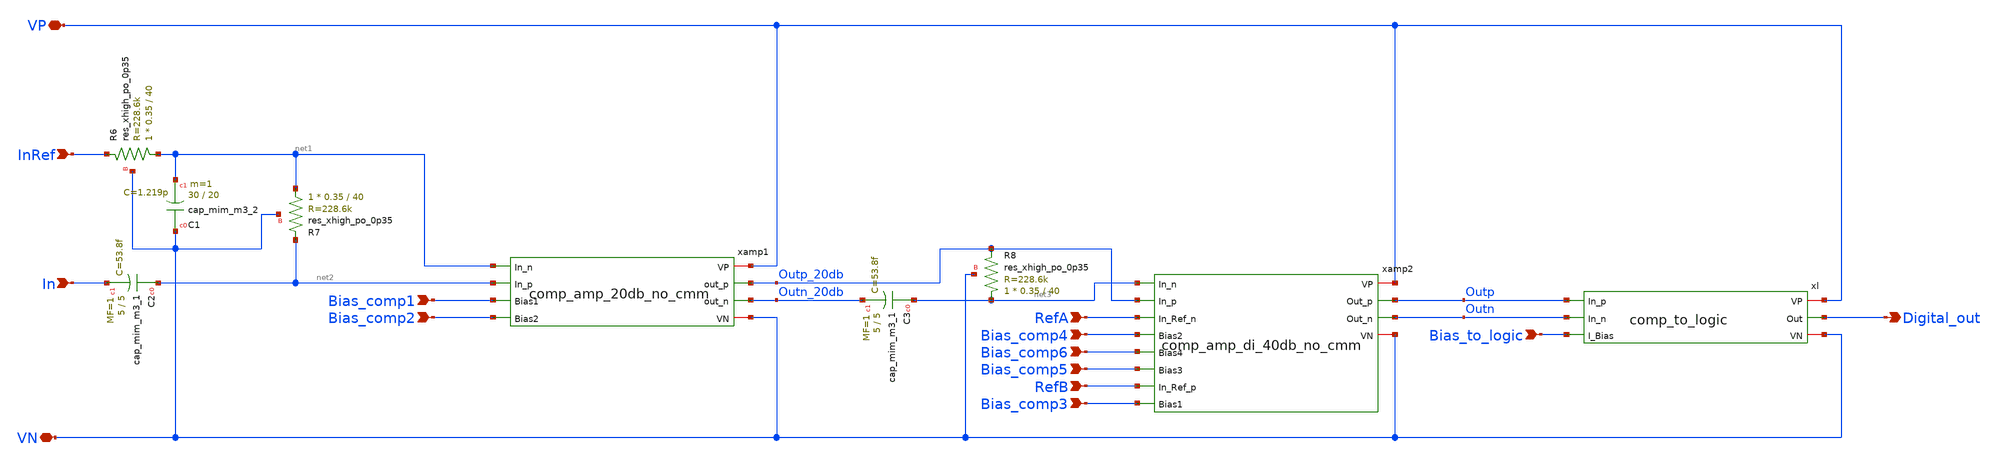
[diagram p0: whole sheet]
** sch_path: xschem/comp/comparator_complete.sch
**.subckt comparator_complete InRef VP Digital_out In Bias_comp1 Bias_comp2 VN Bias_comp4 Bias_comp6
*+ Bias_comp3 Bias_comp5 RefA RefB Bias_to_logic
*.ipin InRef
*.iopin VP
*.opin Digital_out
*.ipin In
*.ipin Bias_comp1
*.ipin Bias_comp2
*.iopin VN
*.ipin Bias_comp4
*.ipin Bias_comp6
*.ipin Bias_comp3
*.ipin Bias_comp5
*.ipin RefA
*.ipin RefB
*.ipin Bias_to_logic
xamp1 VP net1 net2 Outp_20db Bias_comp1 Bias_comp2 Outn_20db VN comp_amp_20db_no_cmm
xl VP Digital_out Outp Outn Bias_to_logic VN comp_to_logic
xamp2 VP net3 Outp_20db Outp RefA Bias_comp4 Bias_comp6 Bias_comp5 Outn RefB Bias_comp3 VN
+ comp_amp_di_40db_no_cmm
XR6 net1 InRef VN sky130_fd_pr__res_xhigh_po_0p35 L=40 mult=1 m=1
XR7 net1 net2 VN sky130_fd_pr__res_xhigh_po_0p35 L=40 mult=1 m=1
XR8 net3 Outp_20db VN sky130_fd_pr__res_xhigh_po_0p35 L=40 mult=1 m=1
XC1 VN net1 sky130_fd_pr__cap_mim_m3_2 W=30 L=20 MF=1 m=1
XC2 net2 In sky130_fd_pr__cap_mim_m3_1 W=5 L=5 MF=1 m=1
XC3 net3 Outn_20db sky130_fd_pr__cap_mim_m3_1 W=5 L=5 MF=1 m=1
**.ends

* expanding   symbol:  comp/comp_amp_20db_no_cmm.sym # of pins=8
** sym_path: xschem/comp/comp_amp_20db_no_cmm.sym
** sch_path: xschem/comp/comp_amp_20db_no_cmm.sch
.subckt comp_amp_20db_no_cmm VP In_n In_p out_p Bias1 Bias2 out_n VN
*.ipin In_n
*.ipin In_p
*.iopin VP
*.opin out_p
*.opin out_n
*.ipin Bias1
*.ipin Bias2
*.iopin VN
xcmp2 VP out_p out_n OutP1 OutN1 Bias2 VN comp_adv3
xcmp1 VP OutP1 OutN1 In_n In_p Bias1 VN comp_adv3
.ends


* expanding   symbol:  comp/comp_to_logic.sym # of pins=6
** sym_path: xschem/comp/comp_to_logic.sym
** sch_path: xschem/comp/comp_to_logic.sch
.subckt comp_to_logic VP Out In_p In_n I_Bias VN
*.iopin VP
*.iopin VN
*.ipin In_p
*.ipin In_n
*.ipin I_Bias
*.opin Out
XM1 VM1D In_n VM4D VN sky130_fd_pr__nfet_01v8_lvt L=0.15 W=2 nf=1 ad='int((nf+1)/2) * W/nf * 0.29' as='int((nf+2)/2) * W/nf * 0.29'
+ pd='2*int((nf+1)/2) * (W/nf + 0.29)' ps='2*int((nf+2)/2) * (W/nf + 0.29)' nrd='0.29 / W' nrs='0.29 / W'
+ sa=0 sb=0 sd=0 mult=2 m=2
XM2 VM1D VM1D VP VP sky130_fd_pr__pfet_01v8 L=0.15 W=2 nf=1 ad='int((nf+1)/2) * W/nf * 0.29' as='int((nf+2)/2) * W/nf * 0.29'
+ pd='2*int((nf+1)/2) * (W/nf + 0.29)' ps='2*int((nf+2)/2) * (W/nf + 0.29)' nrd='0.29 / W' nrs='0.29 / W'
+ sa=0 sb=0 sd=0 mult=2 m=2
XM4 VM4D I_Bias VN VN sky130_fd_pr__nfet_01v8 L=0.3 W=2 nf=1 ad='int((nf+1)/2) * W/nf * 0.29' as='int((nf+2)/2) * W/nf * 0.29'
+ pd='2*int((nf+1)/2) * (W/nf + 0.29)' ps='2*int((nf+2)/2) * (W/nf + 0.29)' nrd='0.29 / W' nrs='0.29 / W'
+ sa=0 sb=0 sd=0 mult=2*8 m=2*8
XM6 VM6D In_p VM4D VN sky130_fd_pr__nfet_01v8_lvt L=0.15 W=2 nf=1 ad='int((nf+1)/2) * W/nf * 0.29' as='int((nf+2)/2) * W/nf * 0.29'
+ pd='2*int((nf+1)/2) * (W/nf + 0.29)' ps='2*int((nf+2)/2) * (W/nf + 0.29)' nrd='0.29 / W' nrs='0.29 / W'
+ sa=0 sb=0 sd=0 mult=2 m=2
XM7 I_Bias I_Bias VN VN sky130_fd_pr__nfet_01v8 L=0.3 W=2 nf=1 ad='int((nf+1)/2) * W/nf * 0.29' as='int((nf+2)/2) * W/nf * 0.29'
+ pd='2*int((nf+1)/2) * (W/nf + 0.29)' ps='2*int((nf+2)/2) * (W/nf + 0.29)' nrd='0.29 / W' nrs='0.29 / W'
+ sa=0 sb=0 sd=0 mult=2 m=2
XM3 VM6D VM6D VP VP sky130_fd_pr__pfet_01v8 L=0.15 W=2 nf=1 ad='int((nf+1)/2) * W/nf * 0.29' as='int((nf+2)/2) * W/nf * 0.29'
+ pd='2*int((nf+1)/2) * (W/nf + 0.29)' ps='2*int((nf+2)/2) * (W/nf + 0.29)' nrd='0.29 / W' nrs='0.29 / W'
+ sa=0 sb=0 sd=0 mult=2 m=2
XM8 VM11D VM1D VP VP sky130_fd_pr__pfet_01v8 L=0.15 W=2 nf=1 ad='int((nf+1)/2) * W/nf * 0.29' as='int((nf+2)/2) * W/nf * 0.29'
+ pd='2*int((nf+1)/2) * (W/nf + 0.29)' ps='2*int((nf+2)/2) * (W/nf + 0.29)' nrd='0.29 / W' nrs='0.29 / W'
+ sa=0 sb=0 sd=0 mult=4 m=4
XM9 VM12D VM6D VP VP sky130_fd_pr__pfet_01v8 L=0.15 W=2 nf=1 ad='int((nf+1)/2) * W/nf * 0.29' as='int((nf+2)/2) * W/nf * 0.29'
+ pd='2*int((nf+1)/2) * (W/nf + 0.29)' ps='2*int((nf+2)/2) * (W/nf + 0.29)' nrd='0.29 / W' nrs='0.29 / W'
+ sa=0 sb=0 sd=0 mult=4 m=4
XM11 VM11D VM11D VN VN sky130_fd_pr__nfet_01v8 L=0.15 W=2 nf=1 ad='int((nf+1)/2) * W/nf * 0.29' as='int((nf+2)/2) * W/nf * 0.29'
+ pd='2*int((nf+1)/2) * (W/nf + 0.29)' ps='2*int((nf+2)/2) * (W/nf + 0.29)' nrd='0.29 / W' nrs='0.29 / W'
+ sa=0 sb=0 sd=0 mult=3 m=3
XM12 VM12D VM11D VN VN sky130_fd_pr__nfet_01v8 L=0.15 W=2 nf=1 ad='int((nf+1)/2) * W/nf * 0.29' as='int((nf+2)/2) * W/nf * 0.29'
+ pd='2*int((nf+1)/2) * (W/nf + 0.29)' ps='2*int((nf+2)/2) * (W/nf + 0.29)' nrd='0.29 / W' nrs='0.29 / W'
+ sa=0 sb=0 sd=0 mult=3 m=3
XM14 VM17D VM12D VP VP sky130_fd_pr__pfet_01v8 L=0.15 W=2 nf=1 ad='int((nf+1)/2) * W/nf * 0.29' as='int((nf+2)/2) * W/nf * 0.29'
+ pd='2*int((nf+1)/2) * (W/nf + 0.29)' ps='2*int((nf+2)/2) * (W/nf + 0.29)' nrd='0.29 / W' nrs='0.29 / W'
+ sa=0 sb=0 sd=0 mult=2 m=2
XM16 VM13D VM17D VP VP sky130_fd_pr__pfet_01v8 L=0.15 W=2 nf=1 ad='int((nf+1)/2) * W/nf * 0.29' as='int((nf+2)/2) * W/nf * 0.29'
+ pd='2*int((nf+1)/2) * (W/nf + 0.29)' ps='2*int((nf+2)/2) * (W/nf + 0.29)' nrd='0.29 / W' nrs='0.29 / W'
+ sa=0 sb=0 sd=0 mult=4 m=4
XM13 VM13D VM17D VN VN sky130_fd_pr__nfet_01v8_lvt L=0.15 W=2 nf=1 ad='int((nf+1)/2) * W/nf * 0.29' as='int((nf+2)/2) * W/nf * 0.29'
+ pd='2*int((nf+1)/2) * (W/nf + 0.29)' ps='2*int((nf+2)/2) * (W/nf + 0.29)' nrd='0.29 / W' nrs='0.29 / W'
+ sa=0 sb=0 sd=0 mult=2 m=2
XM17 VM17D VM12D VN VN sky130_fd_pr__nfet_01v8 L=0.15 W=2 nf=1 ad='int((nf+1)/2) * W/nf * 0.29' as='int((nf+2)/2) * W/nf * 0.29'
+ pd='2*int((nf+1)/2) * (W/nf + 0.29)' ps='2*int((nf+2)/2) * (W/nf + 0.29)' nrd='0.29 / W' nrs='0.29 / W'
+ sa=0 sb=0 sd=0 mult=1 m=1
XM15 VM6D VM1D VP VP sky130_fd_pr__pfet_01v8 L=0.15 W=0.5 nf=1 ad='int((nf+1)/2) * W/nf * 0.29' as='int((nf+2)/2) * W/nf * 0.29'
+ pd='2*int((nf+1)/2) * (W/nf + 0.29)' ps='2*int((nf+2)/2) * (W/nf + 0.29)' nrd='0.29 / W' nrs='0.29 / W'
+ sa=0 sb=0 sd=0 mult=1 m=1
XM19 Out VM13D VP VP sky130_fd_pr__pfet_01v8 L=0.15 W=2 nf=1 ad='int((nf+1)/2) * W/nf * 0.29' as='int((nf+2)/2) * W/nf * 0.29'
+ pd='2*int((nf+1)/2) * (W/nf + 0.29)' ps='2*int((nf+2)/2) * (W/nf + 0.29)' nrd='0.29 / W' nrs='0.29 / W'
+ sa=0 sb=0 sd=0 mult=4 m=4
XM20 Out VM13D VN VN sky130_fd_pr__nfet_01v8_lvt L=0.15 W=2 nf=1 ad='int((nf+1)/2) * W/nf * 0.29' as='int((nf+2)/2) * W/nf * 0.29'
+ pd='2*int((nf+1)/2) * (W/nf + 0.29)' ps='2*int((nf+2)/2) * (W/nf + 0.29)' nrd='0.29 / W' nrs='0.29 / W'
+ sa=0 sb=0 sd=0 mult=2 m=2
XM5 VM1D VM6D VP VP sky130_fd_pr__pfet_01v8 L=0.15 W=0.5 nf=1 ad='int((nf+1)/2) * W/nf * 0.29' as='int((nf+2)/2) * W/nf * 0.29'
+ pd='2*int((nf+1)/2) * (W/nf + 0.29)' ps='2*int((nf+2)/2) * (W/nf + 0.29)' nrd='0.29 / W' nrs='0.29 / W'
+ sa=0 sb=0 sd=0 mult=1 m=1
XM10 VN VN VN VN sky130_fd_pr__nfet_01v8 L=0.3 W=2 nf=1 ad='int((nf+1)/2) * W/nf * 0.29' as='int((nf+2)/2) * W/nf * 0.29'
+ pd='2*int((nf+1)/2) * (W/nf + 0.29)' ps='2*int((nf+2)/2) * (W/nf + 0.29)' nrd='0.29 / W' nrs='0.29 / W'
+ sa=0 sb=0 sd=0 mult=2 m=2
.ends


* expanding   symbol:  comp/comp_amp_di_40db_no_cmm.sym # of pins=12
** sym_path: xschem/comp/comp_amp_di_40db_no_cmm.sym
** sch_path: xschem/comp/comp_amp_di_40db_no_cmm.sch
.subckt comp_amp_di_40db_no_cmm VP In_n In_p Out_p In_Ref_n Bias2 Bias4 Bias3 Out_n In_Ref_p Bias1
+ VN
*.ipin In_n
*.iopin VP
*.opin Out_p
*.ipin In_p
*.ipin Bias1
*.ipin Bias2
*.iopin VN
*.opin Out_n
*.ipin Bias3
*.ipin Bias4
*.ipin In_Ref_n
*.ipin In_Ref_p
xcmp6 VP OutP2_di OutN2_di OutP1_di OutN1_di Bias2 VN comp_adv3
xcmp1 VP OutP3_di OutN3_di OutP2_di OutN2_di Bias3 VN comp_adv3
xcmp2 VP Out_p Out_n OutP3_di OutN3_di Bias4 VN comp_adv3
x1 VP OutP1_di OutN1_di In_n In_p In_Ref_n In_Ref_p Bias1 VN comp_adv3_di
.ends


* expanding   symbol:  comp/comp_adv3.sym # of pins=7
** sym_path: xschem/comp/comp_adv3.sym
** sch_path: xschem/comp/comp_adv3.sch
.subckt comp_adv3 VP OutP OutN Inn Inp bias VN
*.ipin Inp
*.ipin bias
*.ipin Inn
*.iopin VP
*.iopin VN
*.opin OutN
*.opin OutP
XM1 OutN Inp VIq VN sky130_fd_pr__nfet_01v8_lvt L=0.15 W=2 nf=1 ad='int((nf+1)/2) * W/nf * 0.29' as='int((nf+2)/2) * W/nf * 0.29'
+ pd='2*int((nf+1)/2) * (W/nf + 0.29)' ps='2*int((nf+2)/2) * (W/nf + 0.29)' nrd='0.29 / W' nrs='0.29 / W'
+ sa=0 sb=0 sd=0 mult=6 m=6
XM2 OutP Inn VIq VN sky130_fd_pr__nfet_01v8_lvt L=0.15 W=2 nf=1 ad='int((nf+1)/2) * W/nf * 0.29' as='int((nf+2)/2) * W/nf * 0.29'
+ pd='2*int((nf+1)/2) * (W/nf + 0.29)' ps='2*int((nf+2)/2) * (W/nf + 0.29)' nrd='0.29 / W' nrs='0.29 / W'
+ sa=0 sb=0 sd=0 mult=6 m=6
XM7 bias bias VN VN sky130_fd_pr__nfet_01v8_lvt L=0.3 W=2 nf=1 ad='int((nf+1)/2) * W/nf * 0.29' as='int((nf+2)/2) * W/nf * 0.29'
+ pd='2*int((nf+1)/2) * (W/nf + 0.29)' ps='2*int((nf+2)/2) * (W/nf + 0.29)' nrd='0.29 / W' nrs='0.29 / W'
+ sa=0 sb=0 sd=0 mult=1 m=1
XM9 VIq bias VN VN sky130_fd_pr__nfet_01v8_lvt L=0.3 W=2 nf=1 ad='int((nf+1)/2) * W/nf * 0.29' as='int((nf+2)/2) * W/nf * 0.29'
+ pd='2*int((nf+1)/2) * (W/nf + 0.29)' ps='2*int((nf+2)/2) * (W/nf + 0.29)' nrd='0.29 / W' nrs='0.29 / W'
+ sa=0 sb=0 sd=0 mult=10 m=10
XR1 OutN VP VN sky130_fd_pr__res_xhigh_po_2p85 L=1.5 mult=1 m=1
XR2 OutP VP VN sky130_fd_pr__res_xhigh_po_2p85 L=1.5 mult=1 m=1
XM3 bias VN VN VN sky130_fd_pr__nfet_01v8_lvt L=0.3 W=2 nf=1 ad='int((nf+1)/2) * W/nf * 0.29' as='int((nf+2)/2) * W/nf * 0.29'
+ pd='2*int((nf+1)/2) * (W/nf + 0.29)' ps='2*int((nf+2)/2) * (W/nf + 0.29)' nrd='0.29 / W' nrs='0.29 / W'
+ sa=0 sb=0 sd=0 mult=1 m=1
.ends


* expanding   symbol:  comp/comp_adv3_di.sym # of pins=9
** sym_path: xschem/comp/comp_adv3_di.sym
** sch_path: xschem/comp/comp_adv3_di.sch
.subckt comp_adv3_di VP OutP OutN Inn Inp Inn2 Inp2 bias VN
*.ipin Inp
*.ipin bias
*.ipin Inn
*.iopin VP
*.iopin VN
*.opin OutN
*.opin OutP
*.ipin Inn2
*.ipin Inp2
XM1 OutN Inp VIq VN sky130_fd_pr__nfet_01v8_lvt L=0.15 W=2 nf=1 ad='int((nf+1)/2) * W/nf * 0.29' as='int((nf+2)/2) * W/nf * 0.29'
+ pd='2*int((nf+1)/2) * (W/nf + 0.29)' ps='2*int((nf+2)/2) * (W/nf + 0.29)' nrd='0.29 / W' nrs='0.29 / W'
+ sa=0 sb=0 sd=0 mult=6 m=6
XM2 OutP Inn VIq VN sky130_fd_pr__nfet_01v8_lvt L=0.15 W=2 nf=1 ad='int((nf+1)/2) * W/nf * 0.29' as='int((nf+2)/2) * W/nf * 0.29'
+ pd='2*int((nf+1)/2) * (W/nf + 0.29)' ps='2*int((nf+2)/2) * (W/nf + 0.29)' nrd='0.29 / W' nrs='0.29 / W'
+ sa=0 sb=0 sd=0 mult=6 m=6
XM7 bias bias VN VN sky130_fd_pr__nfet_01v8_lvt L=0.3 W=2 nf=1 ad='int((nf+1)/2) * W/nf * 0.29' as='int((nf+2)/2) * W/nf * 0.29'
+ pd='2*int((nf+1)/2) * (W/nf + 0.29)' ps='2*int((nf+2)/2) * (W/nf + 0.29)' nrd='0.29 / W' nrs='0.29 / W'
+ sa=0 sb=0 sd=0 mult=1 m=1
XM9 VIq bias VN VN sky130_fd_pr__nfet_01v8_lvt L=0.3 W=2 nf=1 ad='int((nf+1)/2) * W/nf * 0.29' as='int((nf+2)/2) * W/nf * 0.29'
+ pd='2*int((nf+1)/2) * (W/nf + 0.29)' ps='2*int((nf+2)/2) * (W/nf + 0.29)' nrd='0.29 / W' nrs='0.29 / W'
+ sa=0 sb=0 sd=0 mult=10 m=10
XR1 OutN VP VN sky130_fd_pr__res_xhigh_po_2p85 L=1 mult=1 m=1
XR2 OutP VP VN sky130_fd_pr__res_xhigh_po_2p85 L=1 mult=1 m=1
XM3 OutN Inp2 VN VN sky130_fd_pr__nfet_01v8_lvt L=0.15 W=2 nf=1 ad='int((nf+1)/2) * W/nf * 0.29' as='int((nf+2)/2) * W/nf * 0.29'
+ pd='2*int((nf+1)/2) * (W/nf + 0.29)' ps='2*int((nf+2)/2) * (W/nf + 0.29)' nrd='0.29 / W' nrs='0.29 / W'
+ sa=0 sb=0 sd=0 mult=1 m=1
XM4 OutP Inn2 VN VN sky130_fd_pr__nfet_01v8_lvt L=0.15 W=2 nf=1 ad='int((nf+1)/2) * W/nf * 0.29' as='int((nf+2)/2) * W/nf * 0.29'
+ pd='2*int((nf+1)/2) * (W/nf + 0.29)' ps='2*int((nf+2)/2) * (W/nf + 0.29)' nrd='0.29 / W' nrs='0.29 / W'
+ sa=0 sb=0 sd=0 mult=1 m=1
XM5 Inn2 Inn2 VN VN sky130_fd_pr__nfet_01v8_lvt L=0.15 W=2 nf=1 ad='int((nf+1)/2) * W/nf * 0.29' as='int((nf+2)/2) * W/nf * 0.29'
+ pd='2*int((nf+1)/2) * (W/nf + 0.29)' ps='2*int((nf+2)/2) * (W/nf + 0.29)' nrd='0.29 / W' nrs='0.29 / W'
+ sa=0 sb=0 sd=0 mult=1 m=1
XM6 Inp2 Inp2 VN VN sky130_fd_pr__nfet_01v8_lvt L=0.15 W=2 nf=1 ad='int((nf+1)/2) * W/nf * 0.29' as='int((nf+2)/2) * W/nf * 0.29'
+ pd='2*int((nf+1)/2) * (W/nf + 0.29)' ps='2*int((nf+2)/2) * (W/nf + 0.29)' nrd='0.29 / W' nrs='0.29 / W'
+ sa=0 sb=0 sd=0 mult=1 m=1
XM8 Inp2 VN VN VN sky130_fd_pr__nfet_01v8_lvt L=0.15 W=2 nf=1 ad='int((nf+1)/2) * W/nf * 0.29' as='int((nf+2)/2) * W/nf * 0.29'
+ pd='2*int((nf+1)/2) * (W/nf + 0.29)' ps='2*int((nf+2)/2) * (W/nf + 0.29)' nrd='0.29 / W' nrs='0.29 / W'
+ sa=0 sb=0 sd=0 mult=1 m=1
XM10 Inn2 VN VN VN sky130_fd_pr__nfet_01v8_lvt L=0.15 W=2 nf=1 ad='int((nf+1)/2) * W/nf * 0.29' as='int((nf+2)/2) * W/nf * 0.29'
+ pd='2*int((nf+1)/2) * (W/nf + 0.29)' ps='2*int((nf+2)/2) * (W/nf + 0.29)' nrd='0.29 / W' nrs='0.29 / W'
+ sa=0 sb=0 sd=0 mult=1 m=1
XM11 bias VN VN VN sky130_fd_pr__nfet_01v8_lvt L=0.3 W=2 nf=1 ad='int((nf+1)/2) * W/nf * 0.29' as='int((nf+2)/2) * W/nf * 0.29'
+ pd='2*int((nf+1)/2) * (W/nf + 0.29)' ps='2*int((nf+2)/2) * (W/nf + 0.29)' nrd='0.29 / W' nrs='0.29 / W'
+ sa=0 sb=0 sd=0 mult=1 m=1
.ends

.end
